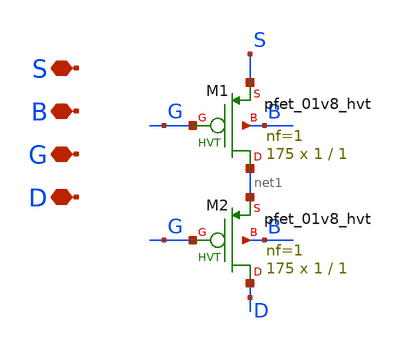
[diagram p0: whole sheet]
** sch_path: xschem/INA/Transistors/transistors_ota_folded/pfet_m1m2_m5_to_m8.sch
**.subckt pfet_m1m2_m5_to_m8 S B G D
*.iopin S
*.iopin B
*.iopin G
*.iopin D
XM1 net1 G S B sky130_fd_pr__pfet_01v8_hvt L=1 W=1 nf=1 ad='int((nf+1)/2) * W/nf * 0.29' as='int((nf+2)/2) * W/nf * 0.29'
+ pd='2*int((nf+1)/2) * (W/nf + 0.29)' ps='2*int((nf+2)/2) * (W/nf + 0.29)' nrd='0.29 / W' nrs='0.29 / W'
+ sa=0 sb=0 sd=0 mult=175 m=175
XM2 D G net1 B sky130_fd_pr__pfet_01v8_hvt L=1 W=1 nf=1 ad='int((nf+1)/2) * W/nf * 0.29' as='int((nf+2)/2) * W/nf * 0.29'
+ pd='2*int((nf+1)/2) * (W/nf + 0.29)' ps='2*int((nf+2)/2) * (W/nf + 0.29)' nrd='0.29 / W' nrs='0.29 / W'
+ sa=0 sb=0 sd=0 mult=175 m=175
**.ends
.end
